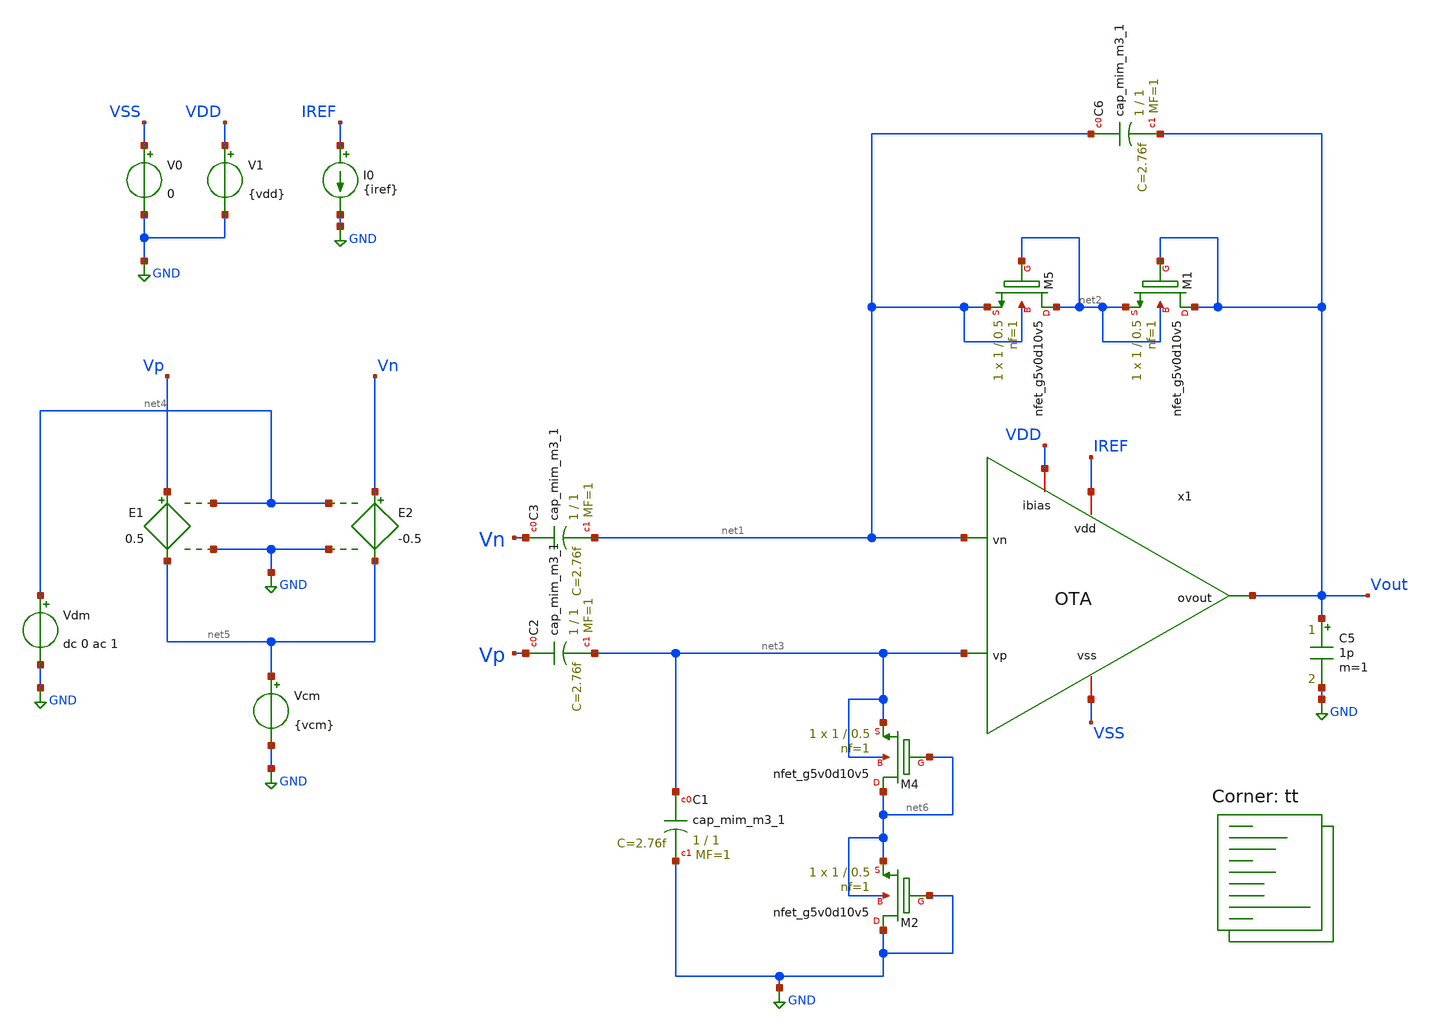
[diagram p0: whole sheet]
** sch_path: xschem/LNA.sch
**.subckt LNA
C5 Vout GND 1p m=1
I0 IREF GND {iref}
V0 VSS GND 0
V1 VDD GND {vdd}
E1 Vp net5 net4 GND 0.5
E2 Vn net5 net4 GND -0.5
Vdm net4 GND dc 0 ac 1
Vcm net5 GND {vcm}
XC6 net1 Vout sky130_fd_pr__cap_mim_m3_1 W=1 L=1 MF=1 m=1
XC1 net3 GND sky130_fd_pr__cap_mim_m3_1 W=1 L=1 MF=1 m=1
XC2 Vp net3 sky130_fd_pr__cap_mim_m3_1 W=1 L=1 MF=1 m=1
XC3 Vn net1 sky130_fd_pr__cap_mim_m3_1 W=1 L=1 MF=1 m=1
x1 Vout IREF VSS VDD net1 net3 OTA
XM5 net2 net2 net1 net1 sky130_fd_pr__nfet_g5v0d10v5 L=0.5 W=1 nf=1 ad='int((nf+1)/2) * W/nf * 0.29'
+ as='int((nf+2)/2) * W/nf * 0.29' pd='2*int((nf+1)/2) * (W/nf + 0.29)' ps='2*int((nf+2)/2) * (W/nf + 0.29)'
+ nrd='0.29 / W' nrs='0.29 / W' sa=0 sb=0 sd=0 mult=1 m=1
XM1 Vout Vout net2 net2 sky130_fd_pr__nfet_g5v0d10v5 L=0.5 W=1 nf=1 ad='int((nf+1)/2) * W/nf * 0.29'
+ as='int((nf+2)/2) * W/nf * 0.29' pd='2*int((nf+1)/2) * (W/nf + 0.29)' ps='2*int((nf+2)/2) * (W/nf + 0.29)'
+ nrd='0.29 / W' nrs='0.29 / W' sa=0 sb=0 sd=0 mult=1 m=1
XM4 net6 net6 net3 net3 sky130_fd_pr__nfet_g5v0d10v5 L=0.5 W=1 nf=1 ad='int((nf+1)/2) * W/nf * 0.29'
+ as='int((nf+2)/2) * W/nf * 0.29' pd='2*int((nf+1)/2) * (W/nf + 0.29)' ps='2*int((nf+2)/2) * (W/nf + 0.29)'
+ nrd='0.29 / W' nrs='0.29 / W' sa=0 sb=0 sd=0 mult=1 m=1
XM2 GND GND net6 net6 sky130_fd_pr__nfet_g5v0d10v5 L=0.5 W=1 nf=1 ad='int((nf+1)/2) * W/nf * 0.29' as='int((nf+2)/2) * W/nf * 0.29'
+ pd='2*int((nf+1)/2) * (W/nf + 0.29)' ps='2*int((nf+2)/2) * (W/nf + 0.29)' nrd='0.29 / W' nrs='0.29 / W'
+ sa=0 sb=0 sd=0 mult=1 m=1
**** begin user architecture code

.param vdd=5
.param vcm=2.5
.param iref = 1m

.control
	save all
	save @m.x1.xm1a.msky130_fd_pr_pfet_g5v0d10v5[id] @m.x1.xm1a.msky130_fd_pr_pfet_g5v0d10v5[gm]
+ @m.x1.xm1a.msky130_fd_pr_pfet_g5v0d10v5[gds]
	save @m.x1.xm1b.msky130_fd_pr_pfet_g5v0d10v5[id] @m.x1.xm1b.msky130_fd_pr_pfet_g5v0d10v5[gm]
+ @m.x1.xm1b.msky130_fd_pr_pfet_g5v0d10v5[gds]
	save @m.x1.xm2a.msky130_fd_pr_pfet_g5v0d10v5[id] @m.x1.xm2a.msky130_fd_pr_pfet_g5v0d10v5[gm]
+ @m.x1.xm2a.msky130_fd_pr_pfet_g5v0d10v5[gds]
	save @m.x1.xm2b.msky130_fd_pr_pfet_g5v0d10v5[id] @m.x1.xm2b.msky130_fd_pr_pfet_g5v0d10v5[gm]
+ @m.x1.xm2b.msky130_fd_pr_pfet_g5v0d10v5[gds]
	save @m.x1.xm3a.msky130_fd_pr_nfet_g5v0d10v5[id] @m.x1.xm3a.msky130_fd_pr_nfet_g5v0d10v5[gm]
+ @m.x1.xm3a.msky130_fd_pr_nfet_g5v0d10v5[gds]
	save @m.x1.xm3b.msky130_fd_pr_nfet_g5v0d10v5[id] @m.x1.xm3b.msky130_fd_pr_nfet_g5v0d10v5[gm]
+ @m.x1.xm3b.msky130_fd_pr_nfet_g5v0d10v5[gds]
	save @m.x1.xm4a.msky130_fd_pr_nfet_g5v0d10v5[id] @m.x1.xm4a.msky130_fd_pr_nfet_g5v0d10v5[gm]
+ @m.x1.xm4a.msky130_fd_pr_nfet_g5v0d10v5[gds]
	save @m.x1.xm4b.msky130_fd_pr_nfet_g5v0d10v5[id] @m.x1.xm4b.msky130_fd_pr_nfet_g5v0d10v5[gm]
+ @m.x1.xm4b.msky130_fd_pr_nfet_g5v0d10v5[gds]
	save @m.x1.xm4c.msky130_fd_pr_nfet_g5v0d10v5[id] @m.x1.xm4c.msky130_fd_pr_nfet_g5v0d10v5[gm]
+ @m.x1.xm4c.msky130_fd_pr_nfet_g5v0d10v5[gds]
	save @m.x1.xm4d.msky130_fd_pr_nfet_g5v0d10v5[id] @m.x1.xm4d.msky130_fd_pr_nfet_g5v0d10v5[gm]
+ @m.x1.xm4d.msky130_fd_pr_nfet_g5v0d10v5[gds]
	save @m.x1.xm5a.msky130_fd_pr_pfet_g5v0d10v5[id] @m.x1.xm5a.msky130_fd_pr_pfet_g5v0d10v5[gm]
+ @m.x1.xm5a.msky130_fd_pr_pfet_g5v0d10v5[gds]
	save @m.x1.xm5b.msky130_fd_pr_pfet_g5v0d10v5[id] @m.x1.xm5b.msky130_fd_pr_pfet_g5v0d10v5[gm]
+ @m.x1.xm5b.msky130_fd_pr_pfet_g5v0d10v5[gds]
	save @m.x1.xm6.msky130_fd_pr_pfet_g5v0d10v5[id] @m.x1.xm6.msky130_fd_pr_pfet_g5v0d10v5[gm]
+ @m.x1.xm6.msky130_fd_pr_pfet_g5v0d10v5[gds]
	save @m.x1.xm7.msky130_fd_pr_pfet_g5v0d10v5[id] @m.x1.xm7.msky130_fd_pr_pfet_g5v0d10v5[gm]
+ @m.x1.xm7.msky130_fd_pr_pfet_g5v0d10v5[gds]

	op
	show

	ac dec 20 0.1 100e9
	let vout_mag = abs(v(Vout))
	print vout_mag
	let vout_phase_margin = phase(v(Vout)) * 180/pi + 180
	meas ac A0 find vout_mag at=1k
	meas ac UGF when vout_mag=1 fall=1
	meas ac PM find vout_phase_margin when vout_mag=1

	echo $plots
	write LNA.raw op1.all

.endc



.lib $::SKYWATER_MODELS/sky130.lib.spice tt
**** end user architecture code
**.ends

* expanding   symbol:  /home/william/projects/sky130_vbl_ip__LNA/xschem/OTA.sym # of pins=6
** sym_path: xschem/OTA.sym
** sch_path: xschem/OTA.sch
.subckt OTA ovout vdd vss ibias vn vp
*.iopin ibias
*.iopin vdd
*.iopin vss
*.ipin vp
*.ipin vn
*.opin ovout
XM5a net2 vp net1 vdd sky130_fd_pr__pfet_g5v0d10v5 L=0.5 W=80 nf=1 ad='int((nf+1)/2) * W/nf * 0.29' as='int((nf+2)/2) * W/nf * 0.29'
+ pd='2*int((nf+1)/2) * (W/nf + 0.29)' ps='2*int((nf+2)/2) * (W/nf + 0.29)' nrd='0.29 / W' nrs='0.29 / W'
+ sa=0 sb=0 sd=0 mult=1 m=1
XM5b net3 vn net1 vdd sky130_fd_pr__pfet_g5v0d10v5 L=0.5 W=80 nf=1 ad='int((nf+1)/2) * W/nf * 0.29' as='int((nf+2)/2) * W/nf * 0.29'
+ pd='2*int((nf+1)/2) * (W/nf + 0.29)' ps='2*int((nf+2)/2) * (W/nf + 0.29)' nrd='0.29 / W' nrs='0.29 / W'
+ sa=0 sb=0 sd=0 mult=1 m=1
XM4b net2 net2 vss vss sky130_fd_pr__nfet_g5v0d10v5 L=4 W=1 nf=1 ad='int((nf+1)/2) * W/nf * 0.29' as='int((nf+2)/2) * W/nf * 0.29'
+ pd='2*int((nf+1)/2) * (W/nf + 0.29)' ps='2*int((nf+2)/2) * (W/nf + 0.29)' nrd='0.29 / W' nrs='0.29 / W'
+ sa=0 sb=0 sd=0 mult=1 m=1
XM4c net3 net3 vss vss sky130_fd_pr__nfet_g5v0d10v5 L=4 W=1 nf=1 ad='int((nf+1)/2) * W/nf * 0.29' as='int((nf+2)/2) * W/nf * 0.29'
+ pd='2*int((nf+1)/2) * (W/nf + 0.29)' ps='2*int((nf+2)/2) * (W/nf + 0.29)' nrd='0.29 / W' nrs='0.29 / W'
+ sa=0 sb=0 sd=0 mult=1 m=1
XM4a net5 net2 vss vss sky130_fd_pr__nfet_g5v0d10v5 L=4 W=1 nf=1 ad='int((nf+1)/2) * W/nf * 0.29' as='int((nf+2)/2) * W/nf * 0.29'
+ pd='2*int((nf+1)/2) * (W/nf + 0.29)' ps='2*int((nf+2)/2) * (W/nf + 0.29)' nrd='0.29 / W' nrs='0.29 / W'
+ sa=0 sb=0 sd=0 mult=1 m=1
XM4d net7 net3 vss vss sky130_fd_pr__nfet_g5v0d10v5 L=4 W=1 nf=1 ad='int((nf+1)/2) * W/nf * 0.29' as='int((nf+2)/2) * W/nf * 0.29'
+ pd='2*int((nf+1)/2) * (W/nf + 0.29)' ps='2*int((nf+2)/2) * (W/nf + 0.29)' nrd='0.29 / W' nrs='0.29 / W'
+ sa=0 sb=0 sd=0 mult=1 m=1
XM1a net4 net4 vdd vdd sky130_fd_pr__pfet_g5v0d10v5 L=1 W=0.6 nf=1 ad='int((nf+1)/2) * W/nf * 0.29' as='int((nf+2)/2) * W/nf * 0.29'
+ pd='2*int((nf+1)/2) * (W/nf + 0.29)' ps='2*int((nf+2)/2) * (W/nf + 0.29)' nrd='0.29 / W' nrs='0.29 / W'
+ sa=0 sb=0 sd=0 mult=1 m=1
XM1b net8 net4 vdd vdd sky130_fd_pr__pfet_g5v0d10v5 L=1 W=0.6 nf=1 ad='int((nf+1)/2) * W/nf * 0.29' as='int((nf+2)/2) * W/nf * 0.29'
+ pd='2*int((nf+1)/2) * (W/nf + 0.29)' ps='2*int((nf+2)/2) * (W/nf + 0.29)' nrd='0.29 / W' nrs='0.29 / W'
+ sa=0 sb=0 sd=0 mult=1 m=1
XM7 ibias ibias vdd vdd sky130_fd_pr__pfet_g5v0d10v5 L=2 W=2 nf=1 ad='int((nf+1)/2) * W/nf * 0.29' as='int((nf+2)/2) * W/nf * 0.29'
+ pd='2*int((nf+1)/2) * (W/nf + 0.29)' ps='2*int((nf+2)/2) * (W/nf + 0.29)' nrd='0.29 / W' nrs='0.29 / W'
+ sa=0 sb=0 sd=0 mult=1 m=1
XM6 net1 ibias vdd vdd sky130_fd_pr__pfet_g5v0d10v5 L=2 W=2 nf=1 ad='int((nf+1)/2) * W/nf * 0.29' as='int((nf+2)/2) * W/nf * 0.29'
+ pd='2*int((nf+1)/2) * (W/nf + 0.29)' ps='2*int((nf+2)/2) * (W/nf + 0.29)' nrd='0.29 / W' nrs='0.29 / W'
+ sa=0 sb=0 sd=0 mult=1 m=1
XM3a net6 net6 net5 vss sky130_fd_pr__nfet_g5v0d10v5 L=4 W=1 nf=1 ad='int((nf+1)/2) * W/nf * 0.29' as='int((nf+2)/2) * W/nf * 0.29'
+ pd='2*int((nf+1)/2) * (W/nf + 0.29)' ps='2*int((nf+2)/2) * (W/nf + 0.29)' nrd='0.29 / W' nrs='0.29 / W'
+ sa=0 sb=0 sd=0 mult=1 m=1
XM2a net6 net6 net4 vdd sky130_fd_pr__pfet_g5v0d10v5 L=1 W=0.6 nf=1 ad='int((nf+1)/2) * W/nf * 0.29'
+ as='int((nf+2)/2) * W/nf * 0.29' pd='2*int((nf+1)/2) * (W/nf + 0.29)' ps='2*int((nf+2)/2) * (W/nf + 0.29)'
+ nrd='0.29 / W' nrs='0.29 / W' sa=0 sb=0 sd=0 mult=1 m=1
XM2b ovout ovout net8 vdd sky130_fd_pr__pfet_g5v0d10v5 L=1 W=0.6 nf=1 ad='int((nf+1)/2) * W/nf * 0.29'
+ as='int((nf+2)/2) * W/nf * 0.29' pd='2*int((nf+1)/2) * (W/nf + 0.29)' ps='2*int((nf+2)/2) * (W/nf + 0.29)'
+ nrd='0.29 / W' nrs='0.29 / W' sa=0 sb=0 sd=0 mult=1 m=1
XM3b ovout ovout net7 vss sky130_fd_pr__nfet_g5v0d10v5 L=4 W=1 nf=1 ad='int((nf+1)/2) * W/nf * 0.29'
+ as='int((nf+2)/2) * W/nf * 0.29' pd='2*int((nf+1)/2) * (W/nf + 0.29)' ps='2*int((nf+2)/2) * (W/nf + 0.29)'
+ nrd='0.29 / W' nrs='0.29 / W' sa=0 sb=0 sd=0 mult=1 m=1
.ends

.GLOBAL GND
.end
